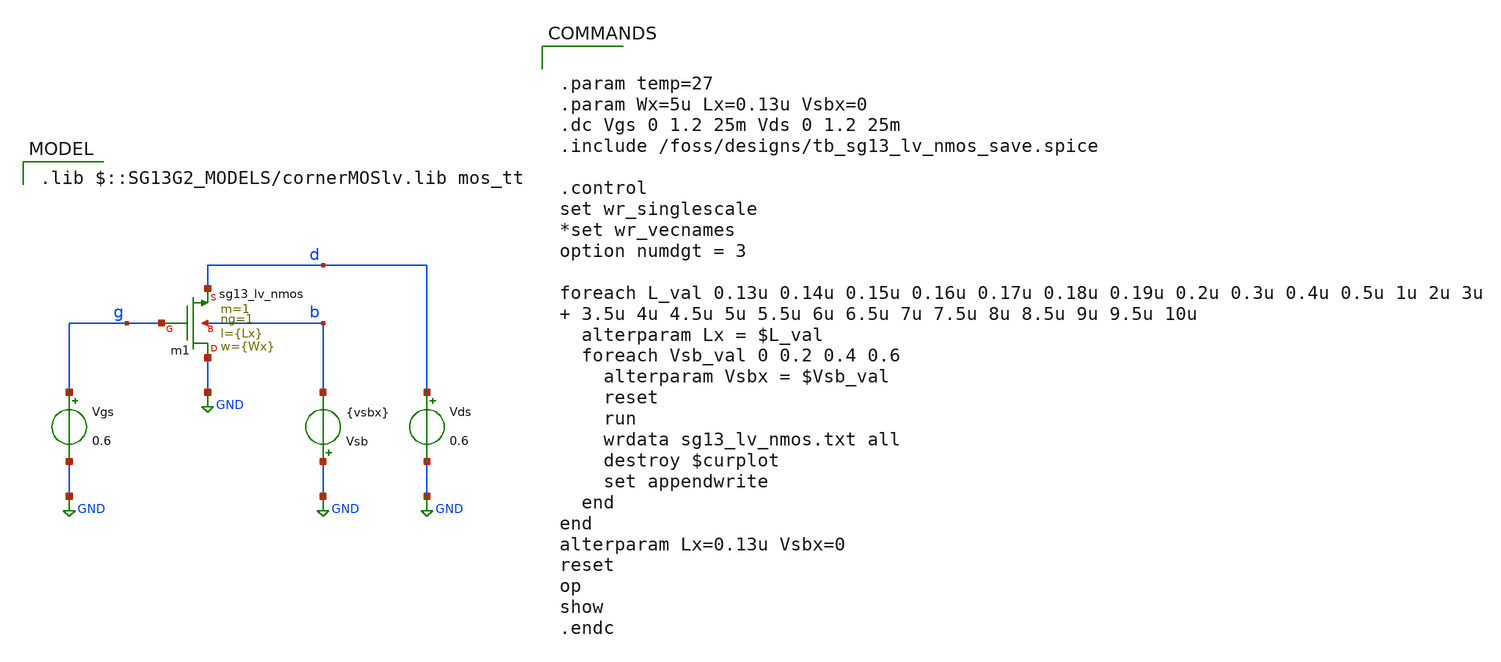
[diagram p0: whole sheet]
** sch_path: 4_Technology/src/tb_sg13_lv_nmos.sch
**.subckt tb_sg13_lv_nmos
Xm1 GND g d b sg13_lv_nmos w={Wx} l={Lx} ng=1 m=1 mm_ok=1
Vgs g GND 0.6
Vds d GND 0.6
Vsb GND b {vsbx}
**** begin user architecture code
 .lib $::SG13G2_MODELS/cornerMOSlv.lib mos_tt



.param temp=27
.param Wx=5u Lx=0.13u Vsbx=0
.dc Vgs 0 1.2 25m Vds 0 1.2 25m
.include /foss/designs/tb_sg13_lv_nmos_save.spice

.control
set wr_singlescale
*set wr_vecnames
option numdgt = 3

foreach L_val 0.13u 0.14u 0.15u 0.16u 0.17u 0.18u 0.19u 0.2u 0.3u 0.4u 0.5u 1u 2u 3u   3.5u 4u 4.5u
+ 5u 5.5u 6u 6.5u 7u 7.5u 8u 8.5u 9u 9.5u 10u
  alterparam Lx = $L_val
  foreach Vsb_val 0 0.2 0.4 0.6
    alterparam Vsbx = $Vsb_val
    reset
    run
    wrdata sg13_lv_nmos.txt all
    destroy $curplot
    set appendwrite
  end
end
alterparam Lx=0.13u Vsbx=0
reset
op
show
.endc


**** end user architecture code
**.ends
.GLOBAL GND
.end
